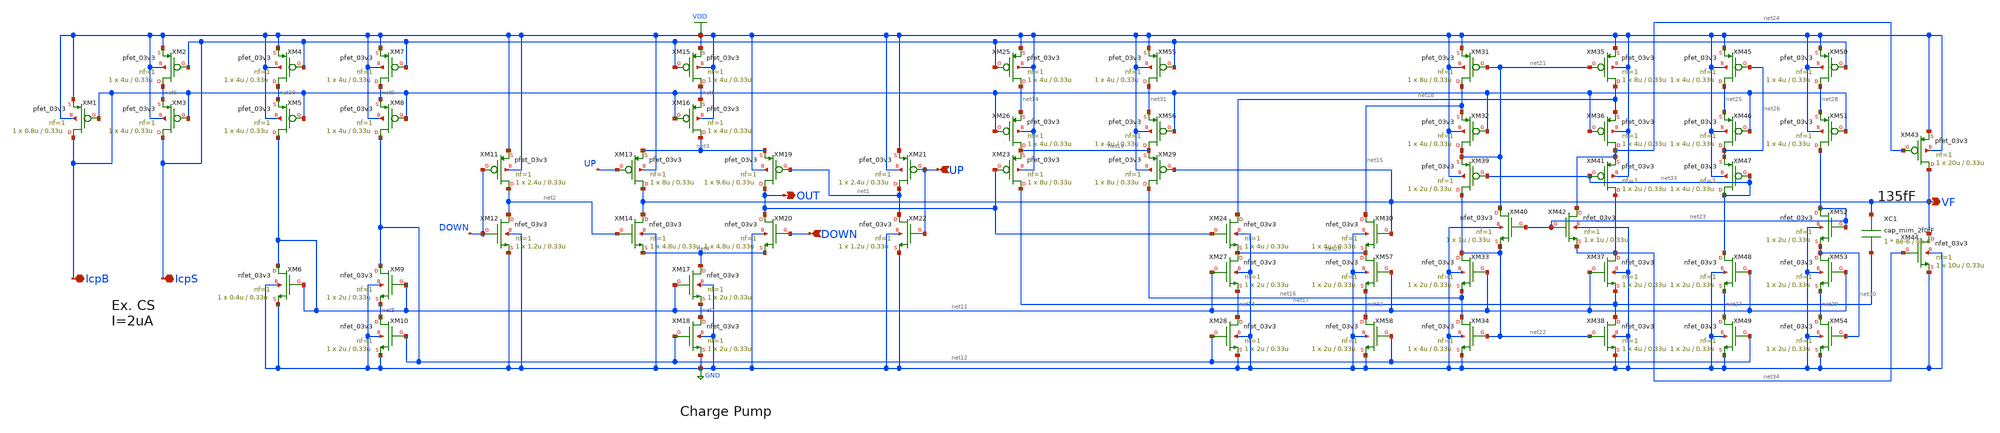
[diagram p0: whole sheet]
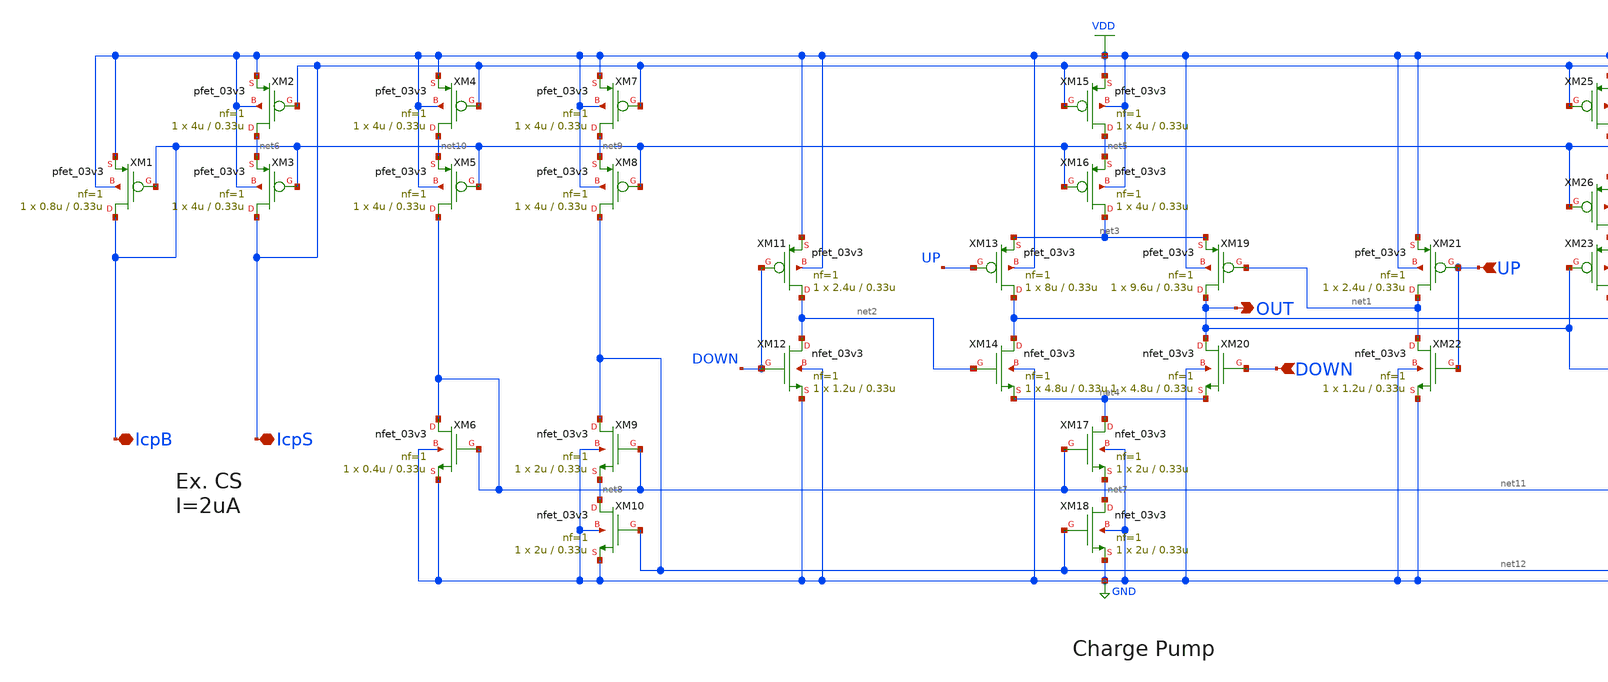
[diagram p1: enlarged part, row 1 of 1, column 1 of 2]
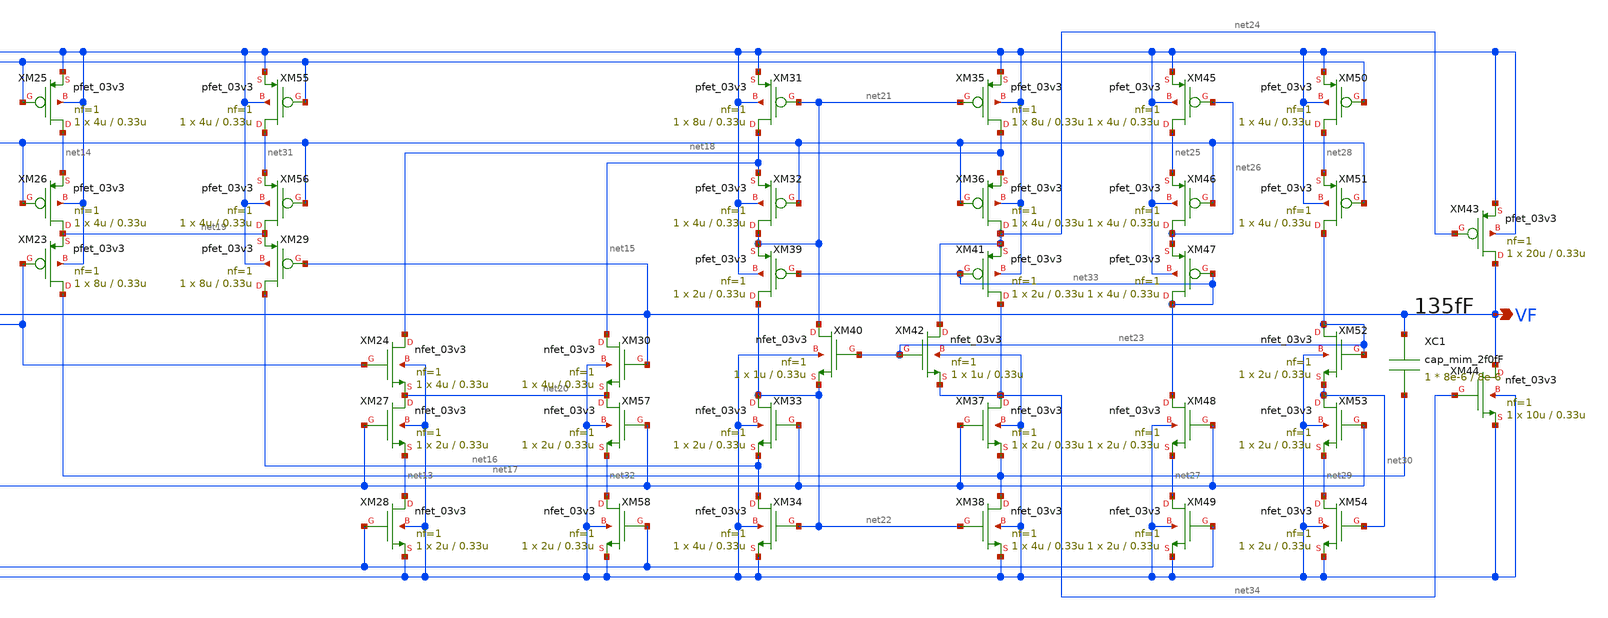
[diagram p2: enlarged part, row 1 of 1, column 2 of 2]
** sch_path: cp.sch
**.subckt cp IcpS IcpB DOWN UP OUT VF
*.iopin IcpS
*.iopin IcpB
*.ipin DOWN
*.ipin UP
*.opin OUT
*.opin VF
XM23 net17 OUT net19 VDD pfet_03v3 L=0.33u W=8u nf=1 ad='int((nf+1)/2) * W/nf * 0.18u' as='int((nf+2)/2) * W/nf * 0.18u'
+ pd='2*int((nf+1)/2) * (W/nf + 0.18u)' ps='2*int((nf+2)/2) * (W/nf + 0.18u)' nrd='0.18u / W' nrs='0.18u / W'
+ sa=0 sb=0 sd=0 m=1
XM29 net16 VF net19 VDD pfet_03v3 L=0.33u W=8u nf=1 ad='int((nf+1)/2) * W/nf * 0.18u' as='int((nf+2)/2) * W/nf * 0.18u'
+ pd='2*int((nf+1)/2) * (W/nf + 0.18u)' ps='2*int((nf+2)/2) * (W/nf + 0.18u)' nrd='0.18u / W' nrs='0.18u / W'
+ sa=0 sb=0 sd=0 m=1
XM19 OUT net1 net3 VDD pfet_03v3 L=0.33u W=9.6u nf=1 ad='int((nf+1)/2) * W/nf * 0.18u' as='int((nf+2)/2) * W/nf * 0.18u'
+ pd='2*int((nf+1)/2) * (W/nf + 0.18u)' ps='2*int((nf+2)/2) * (W/nf + 0.18u)' nrd='0.18u / W' nrs='0.18u / W'
+ sa=0 sb=0 sd=0 m=1
XM20 OUT DOWN net4 GND nfet_03v3 L=0.33u W=4.8u nf=1 ad='int((nf+1)/2) * W/nf * 0.18u' as='int((nf+2)/2) * W/nf * 0.18u'
+ pd='2*int((nf+1)/2) * (W/nf + 0.18u)' ps='2*int((nf+2)/2) * (W/nf + 0.18u)' nrd='0.18u / W' nrs='0.18u / W'
+ sa=0 sb=0 sd=0 m=1
XM21 net1 UP VDD VDD pfet_03v3 L=0.33u W=2.4u nf=1 ad='int((nf+1)/2) * W/nf * 0.18u' as='int((nf+2)/2) * W/nf * 0.18u'
+ pd='2*int((nf+1)/2) * (W/nf + 0.18u)' ps='2*int((nf+2)/2) * (W/nf + 0.18u)' nrd='0.18u / W' nrs='0.18u / W'
+ sa=0 sb=0 sd=0 m=1
XM22 net1 UP GND GND nfet_03v3 L=0.33u W=1.2u nf=1 ad='int((nf+1)/2) * W/nf * 0.18u' as='int((nf+2)/2) * W/nf * 0.18u'
+ pd='2*int((nf+1)/2) * (W/nf + 0.18u)' ps='2*int((nf+2)/2) * (W/nf + 0.18u)' nrd='0.18u / W' nrs='0.18u / W'
+ sa=0 sb=0 sd=0 m=1
XM13 VF UP net3 VDD pfet_03v3 L=0.33u W=8u nf=1 ad='int((nf+1)/2) * W/nf * 0.18u' as='int((nf+2)/2) * W/nf * 0.18u'
+ pd='2*int((nf+1)/2) * (W/nf + 0.18u)' ps='2*int((nf+2)/2) * (W/nf + 0.18u)' nrd='0.18u / W' nrs='0.18u / W'
+ sa=0 sb=0 sd=0 m=1
XM14 VF net2 net4 GND nfet_03v3 L=0.33u W=4.8u nf=1 ad='int((nf+1)/2) * W/nf * 0.18u' as='int((nf+2)/2) * W/nf * 0.18u'
+ pd='2*int((nf+1)/2) * (W/nf + 0.18u)' ps='2*int((nf+2)/2) * (W/nf + 0.18u)' nrd='0.18u / W' nrs='0.18u / W'
+ sa=0 sb=0 sd=0 m=1
XM11 net2 DOWN VDD VDD pfet_03v3 L=0.33u W=2.4u nf=1 ad='int((nf+1)/2) * W/nf * 0.18u' as='int((nf+2)/2) * W/nf * 0.18u'
+ pd='2*int((nf+1)/2) * (W/nf + 0.18u)' ps='2*int((nf+2)/2) * (W/nf + 0.18u)' nrd='0.18u / W' nrs='0.18u / W'
+ sa=0 sb=0 sd=0 m=1
XM12 net2 DOWN GND GND nfet_03v3 L=0.33u W=1.2u nf=1 ad='int((nf+1)/2) * W/nf * 0.18u' as='int((nf+2)/2) * W/nf * 0.18u'
+ pd='2*int((nf+1)/2) * (W/nf + 0.18u)' ps='2*int((nf+2)/2) * (W/nf + 0.18u)' nrd='0.18u / W' nrs='0.18u / W'
+ sa=0 sb=0 sd=0 m=1
XM17 net4 net11 net7 GND nfet_03v3 L=0.33u W=2u nf=1 ad='int((nf+1)/2) * W/nf * 0.18u' as='int((nf+2)/2) * W/nf * 0.18u'
+ pd='2*int((nf+1)/2) * (W/nf + 0.18u)' ps='2*int((nf+2)/2) * (W/nf + 0.18u)' nrd='0.18u / W' nrs='0.18u / W'
+ sa=0 sb=0 sd=0 m=1
XM18 net7 net12 GND GND nfet_03v3 L=0.33u W=2u nf=1 ad='int((nf+1)/2) * W/nf * 0.18u' as='int((nf+2)/2) * W/nf * 0.18u'
+ pd='2*int((nf+1)/2) * (W/nf + 0.18u)' ps='2*int((nf+2)/2) * (W/nf + 0.18u)' nrd='0.18u / W' nrs='0.18u / W'
+ sa=0 sb=0 sd=0 m=1
XM15 net5 IcpS VDD VDD pfet_03v3 L=0.33u W=4u nf=1 ad='int((nf+1)/2) * W/nf * 0.18u' as='int((nf+2)/2) * W/nf * 0.18u'
+ pd='2*int((nf+1)/2) * (W/nf + 0.18u)' ps='2*int((nf+2)/2) * (W/nf + 0.18u)' nrd='0.18u / W' nrs='0.18u / W'
+ sa=0 sb=0 sd=0 m=1
XM16 net3 IcpB net5 VDD pfet_03v3 L=0.33u W=4u nf=1 ad='int((nf+1)/2) * W/nf * 0.18u' as='int((nf+2)/2) * W/nf * 0.18u'
+ pd='2*int((nf+1)/2) * (W/nf + 0.18u)' ps='2*int((nf+2)/2) * (W/nf + 0.18u)' nrd='0.18u / W' nrs='0.18u / W'
+ sa=0 sb=0 sd=0 m=1
XM25 net14 IcpS VDD VDD pfet_03v3 L=0.33u W=4u nf=1 ad='int((nf+1)/2) * W/nf * 0.18u' as='int((nf+2)/2) * W/nf * 0.18u'
+ pd='2*int((nf+1)/2) * (W/nf + 0.18u)' ps='2*int((nf+2)/2) * (W/nf + 0.18u)' nrd='0.18u / W' nrs='0.18u / W'
+ sa=0 sb=0 sd=0 m=1
XM26 net19 IcpB net14 VDD pfet_03v3 L=0.33u W=4u nf=1 ad='int((nf+1)/2) * W/nf * 0.18u' as='int((nf+2)/2) * W/nf * 0.18u'
+ pd='2*int((nf+1)/2) * (W/nf + 0.18u)' ps='2*int((nf+2)/2) * (W/nf + 0.18u)' nrd='0.18u / W' nrs='0.18u / W'
+ sa=0 sb=0 sd=0 m=1
XM2 net6 IcpS VDD VDD pfet_03v3 L=0.33u W=4u nf=1 ad='int((nf+1)/2) * W/nf * 0.18u' as='int((nf+2)/2) * W/nf * 0.18u'
+ pd='2*int((nf+1)/2) * (W/nf + 0.18u)' ps='2*int((nf+2)/2) * (W/nf + 0.18u)' nrd='0.18u / W' nrs='0.18u / W'
+ sa=0 sb=0 sd=0 m=1
XM3 IcpS IcpB net6 VDD pfet_03v3 L=0.33u W=4u nf=1 ad='int((nf+1)/2) * W/nf * 0.18u' as='int((nf+2)/2) * W/nf * 0.18u'
+ pd='2*int((nf+1)/2) * (W/nf + 0.18u)' ps='2*int((nf+2)/2) * (W/nf + 0.18u)' nrd='0.18u / W' nrs='0.18u / W'
+ sa=0 sb=0 sd=0 m=1
XM1 IcpB IcpB VDD VDD pfet_03v3 L=0.33u W=0.8u nf=1 ad='int((nf+1)/2) * W/nf * 0.18u' as='int((nf+2)/2) * W/nf * 0.18u'
+ pd='2*int((nf+1)/2) * (W/nf + 0.18u)' ps='2*int((nf+2)/2) * (W/nf + 0.18u)' nrd='0.18u / W' nrs='0.18u / W'
+ sa=0 sb=0 sd=0 m=1
XM9 net12 net11 net8 GND nfet_03v3 L=0.33u W=2u nf=1 ad='int((nf+1)/2) * W/nf * 0.18u' as='int((nf+2)/2) * W/nf * 0.18u'
+ pd='2*int((nf+1)/2) * (W/nf + 0.18u)' ps='2*int((nf+2)/2) * (W/nf + 0.18u)' nrd='0.18u / W' nrs='0.18u / W'
+ sa=0 sb=0 sd=0 m=1
XM10 net8 net12 GND GND nfet_03v3 L=0.33u W=2u nf=1 ad='int((nf+1)/2) * W/nf * 0.18u' as='int((nf+2)/2) * W/nf * 0.18u'
+ pd='2*int((nf+1)/2) * (W/nf + 0.18u)' ps='2*int((nf+2)/2) * (W/nf + 0.18u)' nrd='0.18u / W' nrs='0.18u / W'
+ sa=0 sb=0 sd=0 m=1
XM7 net9 IcpS VDD VDD pfet_03v3 L=0.33u W=4u nf=1 ad='int((nf+1)/2) * W/nf * 0.18u' as='int((nf+2)/2) * W/nf * 0.18u'
+ pd='2*int((nf+1)/2) * (W/nf + 0.18u)' ps='2*int((nf+2)/2) * (W/nf + 0.18u)' nrd='0.18u / W' nrs='0.18u / W'
+ sa=0 sb=0 sd=0 m=1
XM8 net12 IcpB net9 VDD pfet_03v3 L=0.33u W=4u nf=1 ad='int((nf+1)/2) * W/nf * 0.18u' as='int((nf+2)/2) * W/nf * 0.18u'
+ pd='2*int((nf+1)/2) * (W/nf + 0.18u)' ps='2*int((nf+2)/2) * (W/nf + 0.18u)' nrd='0.18u / W' nrs='0.18u / W'
+ sa=0 sb=0 sd=0 m=1
XM4 net10 IcpS VDD VDD pfet_03v3 L=0.33u W=4u nf=1 ad='int((nf+1)/2) * W/nf * 0.18u' as='int((nf+2)/2) * W/nf * 0.18u'
+ pd='2*int((nf+1)/2) * (W/nf + 0.18u)' ps='2*int((nf+2)/2) * (W/nf + 0.18u)' nrd='0.18u / W' nrs='0.18u / W'
+ sa=0 sb=0 sd=0 m=1
XM5 net11 IcpB net10 VDD pfet_03v3 L=0.33u W=4u nf=1 ad='int((nf+1)/2) * W/nf * 0.18u' as='int((nf+2)/2) * W/nf * 0.18u'
+ pd='2*int((nf+1)/2) * (W/nf + 0.18u)' ps='2*int((nf+2)/2) * (W/nf + 0.18u)' nrd='0.18u / W' nrs='0.18u / W'
+ sa=0 sb=0 sd=0 m=1
XM6 net11 net11 GND GND nfet_03v3 L=0.33u W=0.4u nf=1 ad='int((nf+1)/2) * W/nf * 0.18u' as='int((nf+2)/2) * W/nf * 0.18u'
+ pd='2*int((nf+1)/2) * (W/nf + 0.18u)' ps='2*int((nf+2)/2) * (W/nf + 0.18u)' nrd='0.18u / W' nrs='0.18u / W'
+ sa=0 sb=0 sd=0 m=1
XM33 net22 net11 net16 GND nfet_03v3 L=0.33u W=2u nf=1 ad='int((nf+1)/2) * W/nf * 0.18u' as='int((nf+2)/2) * W/nf * 0.18u'
+ pd='2*int((nf+1)/2) * (W/nf + 0.18u)' ps='2*int((nf+2)/2) * (W/nf + 0.18u)' nrd='0.18u / W' nrs='0.18u / W'
+ sa=0 sb=0 sd=0 m=1
XM31 net15 net21 VDD VDD pfet_03v3 L=0.33u W=8u nf=1 ad='int((nf+1)/2) * W/nf * 0.18u' as='int((nf+2)/2) * W/nf * 0.18u'
+ pd='2*int((nf+1)/2) * (W/nf + 0.18u)' ps='2*int((nf+2)/2) * (W/nf + 0.18u)' nrd='0.18u / W' nrs='0.18u / W'
+ sa=0 sb=0 sd=0 m=1
XM32 net21 IcpB net15 VDD pfet_03v3 L=0.33u W=4u nf=1 ad='int((nf+1)/2) * W/nf * 0.18u' as='int((nf+2)/2) * W/nf * 0.18u'
+ pd='2*int((nf+1)/2) * (W/nf + 0.18u)' ps='2*int((nf+2)/2) * (W/nf + 0.18u)' nrd='0.18u / W' nrs='0.18u / W'
+ sa=0 sb=0 sd=0 m=1
XM34 net16 net22 GND GND nfet_03v3 L=0.33u W=4u nf=1 ad='int((nf+1)/2) * W/nf * 0.18u' as='int((nf+2)/2) * W/nf * 0.18u'
+ pd='2*int((nf+1)/2) * (W/nf + 0.18u)' ps='2*int((nf+2)/2) * (W/nf + 0.18u)' nrd='0.18u / W' nrs='0.18u / W'
+ sa=0 sb=0 sd=0 m=1
XM35 net18 net21 VDD VDD pfet_03v3 L=0.33u W=8u nf=1 ad='int((nf+1)/2) * W/nf * 0.18u' as='int((nf+2)/2) * W/nf * 0.18u'
+ pd='2*int((nf+1)/2) * (W/nf + 0.18u)' ps='2*int((nf+2)/2) * (W/nf + 0.18u)' nrd='0.18u / W' nrs='0.18u / W'
+ sa=0 sb=0 sd=0 m=1
XM36 net24 IcpB net18 VDD pfet_03v3 L=0.33u W=4u nf=1 ad='int((nf+1)/2) * W/nf * 0.18u' as='int((nf+2)/2) * W/nf * 0.18u'
+ pd='2*int((nf+1)/2) * (W/nf + 0.18u)' ps='2*int((nf+2)/2) * (W/nf + 0.18u)' nrd='0.18u / W' nrs='0.18u / W'
+ sa=0 sb=0 sd=0 m=1
XM37 net34 net11 net17 GND nfet_03v3 L=0.33u W=2u nf=1 ad='int((nf+1)/2) * W/nf * 0.18u' as='int((nf+2)/2) * W/nf * 0.18u'
+ pd='2*int((nf+1)/2) * (W/nf + 0.18u)' ps='2*int((nf+2)/2) * (W/nf + 0.18u)' nrd='0.18u / W' nrs='0.18u / W'
+ sa=0 sb=0 sd=0 m=1
XM38 net17 net22 GND GND nfet_03v3 L=0.33u W=4u nf=1 ad='int((nf+1)/2) * W/nf * 0.18u' as='int((nf+2)/2) * W/nf * 0.18u'
+ pd='2*int((nf+1)/2) * (W/nf + 0.18u)' ps='2*int((nf+2)/2) * (W/nf + 0.18u)' nrd='0.18u / W' nrs='0.18u / W'
+ sa=0 sb=0 sd=0 m=1
XM27 net20 net11 net13 GND nfet_03v3 L=0.33u W=2u nf=1 ad='int((nf+1)/2) * W/nf * 0.18u' as='int((nf+2)/2) * W/nf * 0.18u'
+ pd='2*int((nf+1)/2) * (W/nf + 0.18u)' ps='2*int((nf+2)/2) * (W/nf + 0.18u)' nrd='0.18u / W' nrs='0.18u / W'
+ sa=0 sb=0 sd=0 m=1
XM28 net13 net12 GND GND nfet_03v3 L=0.33u W=2u nf=1 ad='int((nf+1)/2) * W/nf * 0.18u' as='int((nf+2)/2) * W/nf * 0.18u'
+ pd='2*int((nf+1)/2) * (W/nf + 0.18u)' ps='2*int((nf+2)/2) * (W/nf + 0.18u)' nrd='0.18u / W' nrs='0.18u / W'
+ sa=0 sb=0 sd=0 m=1
XM24 net18 OUT net20 GND nfet_03v3 L=0.33u W=4u nf=1 ad='int((nf+1)/2) * W/nf * 0.18u' as='int((nf+2)/2) * W/nf * 0.18u'
+ pd='2*int((nf+1)/2) * (W/nf + 0.18u)' ps='2*int((nf+2)/2) * (W/nf + 0.18u)' nrd='0.18u / W' nrs='0.18u / W'
+ sa=0 sb=0 sd=0 m=1
XM30 net15 VF net20 GND nfet_03v3 L=0.33u W=4u nf=1 ad='int((nf+1)/2) * W/nf * 0.18u' as='int((nf+2)/2) * W/nf * 0.18u'
+ pd='2*int((nf+1)/2) * (W/nf + 0.18u)' ps='2*int((nf+2)/2) * (W/nf + 0.18u)' nrd='0.18u / W' nrs='0.18u / W'
+ sa=0 sb=0 sd=0 m=1
XM39 net22 net33 net21 VDD pfet_03v3 L=0.33u W=2u nf=1 ad='int((nf+1)/2) * W/nf * 0.18u' as='int((nf+2)/2) * W/nf * 0.18u'
+ pd='2*int((nf+1)/2) * (W/nf + 0.18u)' ps='2*int((nf+2)/2) * (W/nf + 0.18u)' nrd='0.18u / W' nrs='0.18u / W'
+ sa=0 sb=0 sd=0 m=1
XM40 net21 net23 net22 GND nfet_03v3 L=0.33u W=1u nf=1 ad='int((nf+1)/2) * W/nf * 0.18u' as='int((nf+2)/2) * W/nf * 0.18u'
+ pd='2*int((nf+1)/2) * (W/nf + 0.18u)' ps='2*int((nf+2)/2) * (W/nf + 0.18u)' nrd='0.18u / W' nrs='0.18u / W'
+ sa=0 sb=0 sd=0 m=1
XM41 net34 net33 net24 VDD pfet_03v3 L=0.33u W=2u nf=1 ad='int((nf+1)/2) * W/nf * 0.18u' as='int((nf+2)/2) * W/nf * 0.18u'
+ pd='2*int((nf+1)/2) * (W/nf + 0.18u)' ps='2*int((nf+2)/2) * (W/nf + 0.18u)' nrd='0.18u / W' nrs='0.18u / W'
+ sa=0 sb=0 sd=0 m=1
XM42 net24 net23 net34 GND nfet_03v3 L=0.33u W=1u nf=1 ad='int((nf+1)/2) * W/nf * 0.18u' as='int((nf+2)/2) * W/nf * 0.18u'
+ pd='2*int((nf+1)/2) * (W/nf + 0.18u)' ps='2*int((nf+2)/2) * (W/nf + 0.18u)' nrd='0.18u / W' nrs='0.18u / W'
+ sa=0 sb=0 sd=0 m=1
XM43 VF net24 VDD VDD pfet_03v3 L=0.33u W=20u nf=1 ad='int((nf+1)/2) * W/nf * 0.18u' as='int((nf+2)/2) * W/nf * 0.18u'
+ pd='2*int((nf+1)/2) * (W/nf + 0.18u)' ps='2*int((nf+2)/2) * (W/nf + 0.18u)' nrd='0.18u / W' nrs='0.18u / W'
+ sa=0 sb=0 sd=0 m=1
XM45 net25 net26 VDD VDD pfet_03v3 L=0.33u W=4u nf=1 ad='int((nf+1)/2) * W/nf * 0.18u' as='int((nf+2)/2) * W/nf * 0.18u'
+ pd='2*int((nf+1)/2) * (W/nf + 0.18u)' ps='2*int((nf+2)/2) * (W/nf + 0.18u)' nrd='0.18u / W' nrs='0.18u / W'
+ sa=0 sb=0 sd=0 m=1
XM46 net26 IcpB net25 VDD pfet_03v3 L=0.33u W=4u nf=1 ad='int((nf+1)/2) * W/nf * 0.18u' as='int((nf+2)/2) * W/nf * 0.18u'
+ pd='2*int((nf+1)/2) * (W/nf + 0.18u)' ps='2*int((nf+2)/2) * (W/nf + 0.18u)' nrd='0.18u / W' nrs='0.18u / W'
+ sa=0 sb=0 sd=0 m=1
XM47 net33 net33 net26 VDD pfet_03v3 L=0.33u W=4u nf=1 ad='int((nf+1)/2) * W/nf * 0.18u' as='int((nf+2)/2) * W/nf * 0.18u'
+ pd='2*int((nf+1)/2) * (W/nf + 0.18u)' ps='2*int((nf+2)/2) * (W/nf + 0.18u)' nrd='0.18u / W' nrs='0.18u / W'
+ sa=0 sb=0 sd=0 m=1
XM48 net33 net11 net27 GND nfet_03v3 L=0.33u W=2u nf=1 ad='int((nf+1)/2) * W/nf * 0.18u' as='int((nf+2)/2) * W/nf * 0.18u'
+ pd='2*int((nf+1)/2) * (W/nf + 0.18u)' ps='2*int((nf+2)/2) * (W/nf + 0.18u)' nrd='0.18u / W' nrs='0.18u / W'
+ sa=0 sb=0 sd=0 m=1
XM49 net27 net12 GND GND nfet_03v3 L=0.33u W=2u nf=1 ad='int((nf+1)/2) * W/nf * 0.18u' as='int((nf+2)/2) * W/nf * 0.18u'
+ pd='2*int((nf+1)/2) * (W/nf + 0.18u)' ps='2*int((nf+2)/2) * (W/nf + 0.18u)' nrd='0.18u / W' nrs='0.18u / W'
+ sa=0 sb=0 sd=0 m=1
XM50 net28 IcpS VDD VDD pfet_03v3 L=0.33u W=4u nf=1 ad='int((nf+1)/2) * W/nf * 0.18u' as='int((nf+2)/2) * W/nf * 0.18u'
+ pd='2*int((nf+1)/2) * (W/nf + 0.18u)' ps='2*int((nf+2)/2) * (W/nf + 0.18u)' nrd='0.18u / W' nrs='0.18u / W'
+ sa=0 sb=0 sd=0 m=1
XM51 net23 IcpB net28 VDD pfet_03v3 L=0.33u W=4u nf=1 ad='int((nf+1)/2) * W/nf * 0.18u' as='int((nf+2)/2) * W/nf * 0.18u'
+ pd='2*int((nf+1)/2) * (W/nf + 0.18u)' ps='2*int((nf+2)/2) * (W/nf + 0.18u)' nrd='0.18u / W' nrs='0.18u / W'
+ sa=0 sb=0 sd=0 m=1
XM53 net30 net11 net29 GND nfet_03v3 L=0.33u W=2u nf=1 ad='int((nf+1)/2) * W/nf * 0.18u' as='int((nf+2)/2) * W/nf * 0.18u'
+ pd='2*int((nf+1)/2) * (W/nf + 0.18u)' ps='2*int((nf+2)/2) * (W/nf + 0.18u)' nrd='0.18u / W' nrs='0.18u / W'
+ sa=0 sb=0 sd=0 m=1
XM54 net29 net30 GND GND nfet_03v3 L=0.33u W=2u nf=1 ad='int((nf+1)/2) * W/nf * 0.18u' as='int((nf+2)/2) * W/nf * 0.18u'
+ pd='2*int((nf+1)/2) * (W/nf + 0.18u)' ps='2*int((nf+2)/2) * (W/nf + 0.18u)' nrd='0.18u / W' nrs='0.18u / W'
+ sa=0 sb=0 sd=0 m=1
XM52 net23 net23 net30 GND nfet_03v3 L=0.33u W=2u nf=1 ad='int((nf+1)/2) * W/nf * 0.18u' as='int((nf+2)/2) * W/nf * 0.18u'
+ pd='2*int((nf+1)/2) * (W/nf + 0.18u)' ps='2*int((nf+2)/2) * (W/nf + 0.18u)' nrd='0.18u / W' nrs='0.18u / W'
+ sa=0 sb=0 sd=0 m=1
XM44 VF net34 GND GND nfet_03v3 L=0.33u W=10u nf=1 ad='int((nf+1)/2) * W/nf * 0.18u' as='int((nf+2)/2) * W/nf * 0.18u'
+ pd='2*int((nf+1)/2) * (W/nf + 0.18u)' ps='2*int((nf+2)/2) * (W/nf + 0.18u)' nrd='0.18u / W' nrs='0.18u / W'
+ sa=0 sb=0 sd=0 m=1
XM55 net31 IcpS VDD VDD pfet_03v3 L=0.33u W=4u nf=1 ad='int((nf+1)/2) * W/nf * 0.18u' as='int((nf+2)/2) * W/nf * 0.18u'
+ pd='2*int((nf+1)/2) * (W/nf + 0.18u)' ps='2*int((nf+2)/2) * (W/nf + 0.18u)' nrd='0.18u / W' nrs='0.18u / W'
+ sa=0 sb=0 sd=0 m=1
XM56 net19 IcpB net31 VDD pfet_03v3 L=0.33u W=4u nf=1 ad='int((nf+1)/2) * W/nf * 0.18u' as='int((nf+2)/2) * W/nf * 0.18u'
+ pd='2*int((nf+1)/2) * (W/nf + 0.18u)' ps='2*int((nf+2)/2) * (W/nf + 0.18u)' nrd='0.18u / W' nrs='0.18u / W'
+ sa=0 sb=0 sd=0 m=1
XM57 net20 net11 net32 GND nfet_03v3 L=0.33u W=2u nf=1 ad='int((nf+1)/2) * W/nf * 0.18u' as='int((nf+2)/2) * W/nf * 0.18u'
+ pd='2*int((nf+1)/2) * (W/nf + 0.18u)' ps='2*int((nf+2)/2) * (W/nf + 0.18u)' nrd='0.18u / W' nrs='0.18u / W'
+ sa=0 sb=0 sd=0 m=1
XM58 net32 net12 GND GND nfet_03v3 L=0.33u W=2u nf=1 ad='int((nf+1)/2) * W/nf * 0.18u' as='int((nf+2)/2) * W/nf * 0.18u'
+ pd='2*int((nf+1)/2) * (W/nf + 0.18u)' ps='2*int((nf+2)/2) * (W/nf + 0.18u)' nrd='0.18u / W' nrs='0.18u / W'
+ sa=0 sb=0 sd=0 m=1
XC1 VF net17 cap_mim_2f0fF c_width=8e-6 c_length=8e-6 m=1
**.ends
.GLOBAL VDD
.GLOBAL GND
.end
